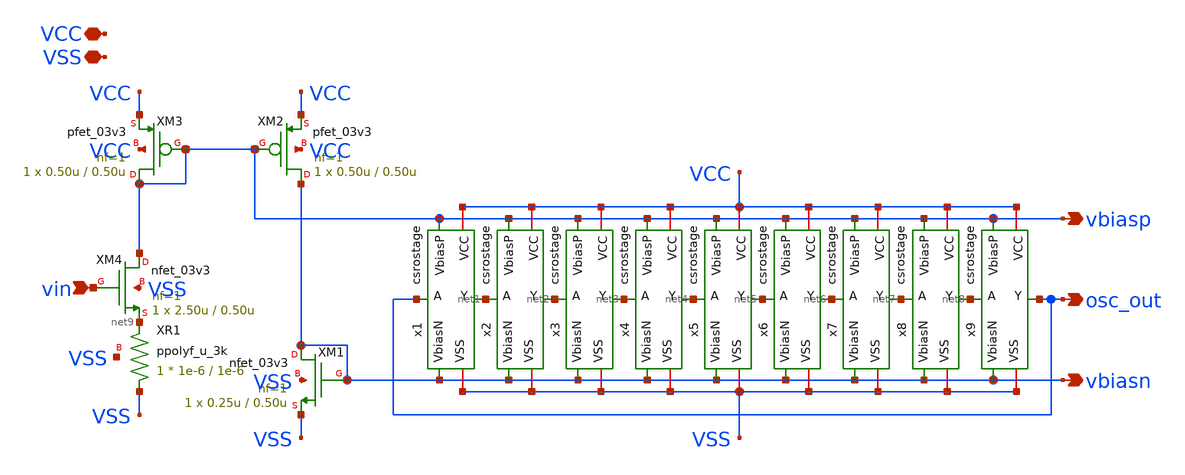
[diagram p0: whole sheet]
** sch_path: xschem/csringosc.sch
**.subckt csringosc osc_out vin VCC VSS vbiasp vbiasn
*.opin osc_out
*.ipin vin
*.iopin VCC
*.iopin VSS
*.opin vbiasp
*.opin vbiasn
x1 VCC VSS vbiasp osc_out net1 vbiasn csrostage
x2 VCC VSS vbiasp net1 net2 vbiasn csrostage
x3 VCC VSS vbiasp net2 net3 vbiasn csrostage
x4 VCC VSS vbiasp net3 net4 vbiasn csrostage
x5 VCC VSS vbiasp net4 net5 vbiasn csrostage
x6 VCC VSS vbiasp net5 net6 vbiasn csrostage
x7 VCC VSS vbiasp net6 net7 vbiasn csrostage
x8 VCC VSS vbiasp net7 net8 vbiasn csrostage
x9 VCC VSS vbiasp net8 osc_out vbiasn csrostage
XM1 vbiasn vbiasn VSS VSS nfet_03v3 L=0.50u W=0.25u nf=1 ad='int((nf+1)/2) * W/nf * 0.18u' as='int((nf+2)/2) * W/nf * 0.18u'
+ pd='2*int((nf+1)/2) * (W/nf + 0.18u)' ps='2*int((nf+2)/2) * (W/nf + 0.18u)' nrd='0.18u / W' nrs='0.18u / W'
+ sa=0 sb=0 sd=0 m=1
XM2 vbiasn vbiasp VCC VCC pfet_03v3 L=0.50u W=0.50u nf=1 ad='int((nf+1)/2) * W/nf * 0.18u' as='int((nf+2)/2) * W/nf * 0.18u'
+ pd='2*int((nf+1)/2) * (W/nf + 0.18u)' ps='2*int((nf+2)/2) * (W/nf + 0.18u)' nrd='0.18u / W' nrs='0.18u / W'
+ sa=0 sb=0 sd=0 m=1
XM3 vbiasp vbiasp VCC VCC pfet_03v3 L=0.50u W=0.50u nf=1 ad='int((nf+1)/2) * W/nf * 0.18u' as='int((nf+2)/2) * W/nf * 0.18u'
+ pd='2*int((nf+1)/2) * (W/nf + 0.18u)' ps='2*int((nf+2)/2) * (W/nf + 0.18u)' nrd='0.18u / W' nrs='0.18u / W'
+ sa=0 sb=0 sd=0 m=1
XM4 vbiasp vin net9 VSS nfet_03v3 L=0.50u W=2.50u nf=1 ad='int((nf+1)/2) * W/nf * 0.18u' as='int((nf+2)/2) * W/nf * 0.18u'
+ pd='2*int((nf+1)/2) * (W/nf + 0.18u)' ps='2*int((nf+2)/2) * (W/nf + 0.18u)' nrd='0.18u / W' nrs='0.18u / W'
+ sa=0 sb=0 sd=0 m=1
XR1 VSS net9 VSS ppolyf_u_3k r_width=1e-6 r_length=1e-6 m=1
**.ends

* expanding   symbol:  csrostage.sym # of pins=6
** sym_path: xschem/csrostage.sym
** sch_path: xschem/csrostage.sch
.subckt csrostage VCC VSS VbiasP A Y VbiasN
*.iopin VCC
*.iopin VSS
*.ipin A
*.opin Y
*.ipin VbiasP
*.ipin VbiasN
XM1 Y A net1 VSS nfet_03v3 L=0.50u W=0.25u nf=1 ad='int((nf+1)/2) * W/nf * 0.18u' as='int((nf+2)/2) * W/nf * 0.18u'
+ pd='2*int((nf+1)/2) * (W/nf + 0.18u)' ps='2*int((nf+2)/2) * (W/nf + 0.18u)' nrd='0.18u / W' nrs='0.18u / W'
+ sa=0 sb=0 sd=0 m=1
XM2 Y A net2 VCC pfet_03v3 L=0.50u W=0.50u nf=1 ad='int((nf+1)/2) * W/nf * 0.18u' as='int((nf+2)/2) * W/nf * 0.18u'
+ pd='2*int((nf+1)/2) * (W/nf + 0.18u)' ps='2*int((nf+2)/2) * (W/nf + 0.18u)' nrd='0.18u / W' nrs='0.18u / W'
+ sa=0 sb=0 sd=0 m=1
XM3 net2 VbiasP VCC VCC pfet_03v3 L=0.50u W=0.50u nf=1 ad='int((nf+1)/2) * W/nf * 0.18u' as='int((nf+2)/2) * W/nf * 0.18u'
+ pd='2*int((nf+1)/2) * (W/nf + 0.18u)' ps='2*int((nf+2)/2) * (W/nf + 0.18u)' nrd='0.18u / W' nrs='0.18u / W'
+ sa=0 sb=0 sd=0 m=1
XM4 net1 VbiasN VSS VSS nfet_03v3 L=0.50u W=0.25u nf=1 ad='int((nf+1)/2) * W/nf * 0.18u' as='int((nf+2)/2) * W/nf * 0.18u'
+ pd='2*int((nf+1)/2) * (W/nf + 0.18u)' ps='2*int((nf+2)/2) * (W/nf + 0.18u)' nrd='0.18u / W' nrs='0.18u / W'
+ sa=0 sb=0 sd=0 m=1
.ends

.end
